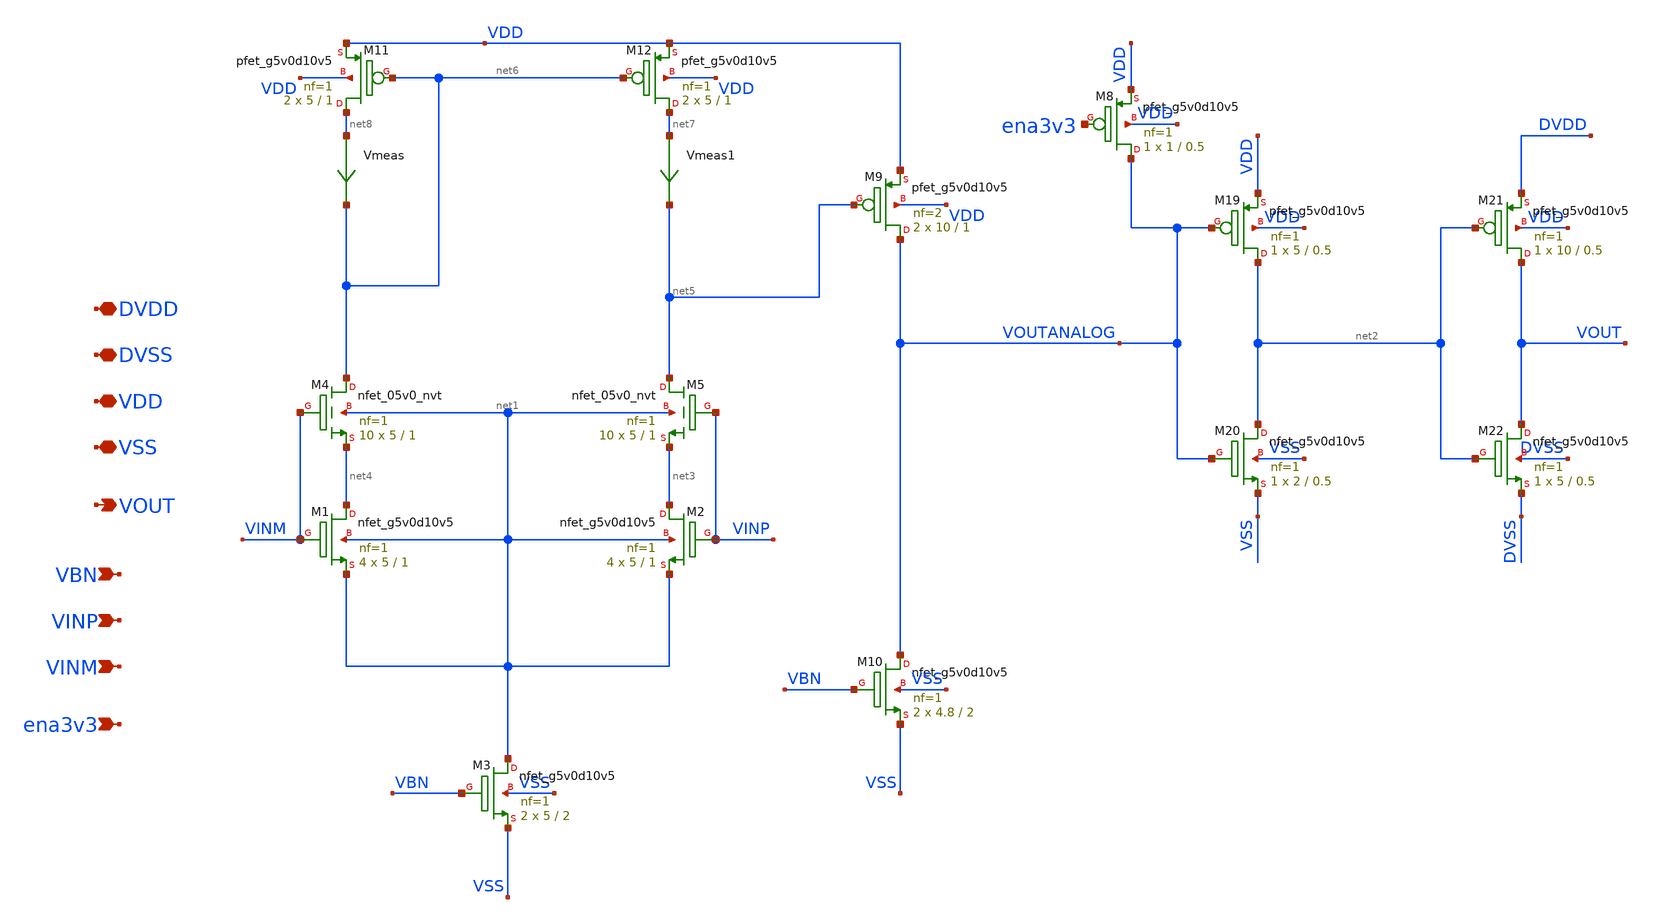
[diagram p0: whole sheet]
** sch_path: xschem/comparator_high_gain.sch
**.subckt comparator_high_gain VINP VINM VBN VDD VSS VOUT DVDD ena3v3 DVSS
*.ipin VINP
*.ipin VINM
*.ipin VBN
*.iopin VDD
*.iopin VSS
*.opin VOUT
*.iopin DVDD
*.ipin ena3v3
*.iopin DVSS
XM3 net1 VBN VSS VSS sky130_fd_pr__nfet_g5v0d10v5 L=2 W=5 nf=1 ad='int((nf+1)/2) * W/nf * 0.29' as='int((nf+2)/2) * W/nf * 0.29'
+ pd='2*int((nf+1)/2) * (W/nf + 0.29)' ps='2*int((nf+2)/2) * (W/nf + 0.29)' nrd='0.29 / W' nrs='0.29 / W'
+ sa=0 sb=0 sd=0 mult=2 m=2
XM19 net2 VOUTANALOG VDD VDD sky130_fd_pr__pfet_g5v0d10v5 L=0.5 W=5 nf=1 ad='int((nf+1)/2) * W/nf * 0.29'
+ as='int((nf+2)/2) * W/nf * 0.29' pd='2*int((nf+1)/2) * (W/nf + 0.29)' ps='2*int((nf+2)/2) * (W/nf + 0.29)'
+ nrd='0.29 / W' nrs='0.29 / W' sa=0 sb=0 sd=0 mult=1 m=1
XM20 net2 VOUTANALOG VSS VSS sky130_fd_pr__nfet_g5v0d10v5 L=0.5 W=2 nf=1 ad='int((nf+1)/2) * W/nf * 0.29'
+ as='int((nf+2)/2) * W/nf * 0.29' pd='2*int((nf+1)/2) * (W/nf + 0.29)' ps='2*int((nf+2)/2) * (W/nf + 0.29)'
+ nrd='0.29 / W' nrs='0.29 / W' sa=0 sb=0 sd=0 mult=1 m=1
XM21 VOUT net2 DVDD VDD sky130_fd_pr__pfet_g5v0d10v5 L=0.5 W=10 nf=1 ad='int((nf+1)/2) * W/nf * 0.29'
+ as='int((nf+2)/2) * W/nf * 0.29' pd='2*int((nf+1)/2) * (W/nf + 0.29)' ps='2*int((nf+2)/2) * (W/nf + 0.29)'
+ nrd='0.29 / W' nrs='0.29 / W' sa=0 sb=0 sd=0 mult=1 m=1
XM22 VOUT net2 DVSS DVSS sky130_fd_pr__nfet_g5v0d10v5 L=0.5 W=5 nf=1 ad='int((nf+1)/2) * W/nf * 0.29'
+ as='int((nf+2)/2) * W/nf * 0.29' pd='2*int((nf+1)/2) * (W/nf + 0.29)' ps='2*int((nf+2)/2) * (W/nf + 0.29)'
+ nrd='0.29 / W' nrs='0.29 / W' sa=0 sb=0 sd=0 mult=1 m=1
XM1 net4 VINM net1 net1 sky130_fd_pr__nfet_g5v0d10v5 L=1 W=5 nf=1 ad='int((nf+1)/2) * W/nf * 0.29' as='int((nf+2)/2) * W/nf * 0.29'
+ pd='2*int((nf+1)/2) * (W/nf + 0.29)' ps='2*int((nf+2)/2) * (W/nf + 0.29)' nrd='0.29 / W' nrs='0.29 / W'
+ sa=0 sb=0 sd=0 mult=4 m=4
XM2 net3 VINP net1 net1 sky130_fd_pr__nfet_g5v0d10v5 L=1 W=5 nf=1 ad='int((nf+1)/2) * W/nf * 0.29' as='int((nf+2)/2) * W/nf * 0.29'
+ pd='2*int((nf+1)/2) * (W/nf + 0.29)' ps='2*int((nf+2)/2) * (W/nf + 0.29)' nrd='0.29 / W' nrs='0.29 / W'
+ sa=0 sb=0 sd=0 mult=4 m=4
XM4 net6 VINM net4 net1 sky130_fd_pr__nfet_05v0_nvt L=1 W=5 nf=1 ad='int((nf+1)/2) * W/nf * 0.29' as='int((nf+2)/2) * W/nf * 0.29'
+ pd='2*int((nf+1)/2) * (W/nf + 0.29)' ps='2*int((nf+2)/2) * (W/nf + 0.29)' nrd='0.29 / W' nrs='0.29 / W'
+ sa=0 sb=0 sd=0 mult=10 m=10
XM5 net5 VINP net3 net1 sky130_fd_pr__nfet_05v0_nvt L=1 W=5 nf=1 ad='int((nf+1)/2) * W/nf * 0.29' as='int((nf+2)/2) * W/nf * 0.29'
+ pd='2*int((nf+1)/2) * (W/nf + 0.29)' ps='2*int((nf+2)/2) * (W/nf + 0.29)' nrd='0.29 / W' nrs='0.29 / W'
+ sa=0 sb=0 sd=0 mult=10 m=10
XM8 VOUTANALOG ena3v3 VDD VDD sky130_fd_pr__pfet_g5v0d10v5 L=0.5 W=1 nf=1 ad='int((nf+1)/2) * W/nf * 0.29'
+ as='int((nf+2)/2) * W/nf * 0.29' pd='2*int((nf+1)/2) * (W/nf + 0.29)' ps='2*int((nf+2)/2) * (W/nf + 0.29)'
+ nrd='0.29 / W' nrs='0.29 / W' sa=0 sb=0 sd=0 mult=1 m=1
XM9 VOUTANALOG net5 VDD VDD sky130_fd_pr__pfet_g5v0d10v5 L=1 W=10 nf=2 ad='int((nf+1)/2) * W/nf * 0.29'
+ as='int((nf+2)/2) * W/nf * 0.29' pd='2*int((nf+1)/2) * (W/nf + 0.29)' ps='2*int((nf+2)/2) * (W/nf + 0.29)'
+ nrd='0.29 / W' nrs='0.29 / W' sa=0 sb=0 sd=0 mult=2 m=2
XM10 VOUTANALOG VBN VSS VSS sky130_fd_pr__nfet_g5v0d10v5 L=2 W=4.8 nf=1 ad='int((nf+1)/2) * W/nf * 0.29'
+ as='int((nf+2)/2) * W/nf * 0.29' pd='2*int((nf+1)/2) * (W/nf + 0.29)' ps='2*int((nf+2)/2) * (W/nf + 0.29)'
+ nrd='0.29 / W' nrs='0.29 / W' sa=0 sb=0 sd=0 mult=2 m=2
XM11 net8 net6 VDD VDD sky130_fd_pr__pfet_g5v0d10v5 L=1 W=5 nf=1 ad='int((nf+1)/2) * W/nf * 0.29' as='int((nf+2)/2) * W/nf * 0.29'
+ pd='2*int((nf+1)/2) * (W/nf + 0.29)' ps='2*int((nf+2)/2) * (W/nf + 0.29)' nrd='0.29 / W' nrs='0.29 / W'
+ sa=0 sb=0 sd=0 mult=2 m=2
XM12 net7 net6 VDD VDD sky130_fd_pr__pfet_g5v0d10v5 L=1 W=5 nf=1 ad='int((nf+1)/2) * W/nf * 0.29' as='int((nf+2)/2) * W/nf * 0.29'
+ pd='2*int((nf+1)/2) * (W/nf + 0.29)' ps='2*int((nf+2)/2) * (W/nf + 0.29)' nrd='0.29 / W' nrs='0.29 / W'
+ sa=0 sb=0 sd=0 mult=2 m=2
Vmeas net8 net6 0
.save i(vmeas)
Vmeas1 net7 net5 0
.save i(vmeas1)
**.ends
.end
